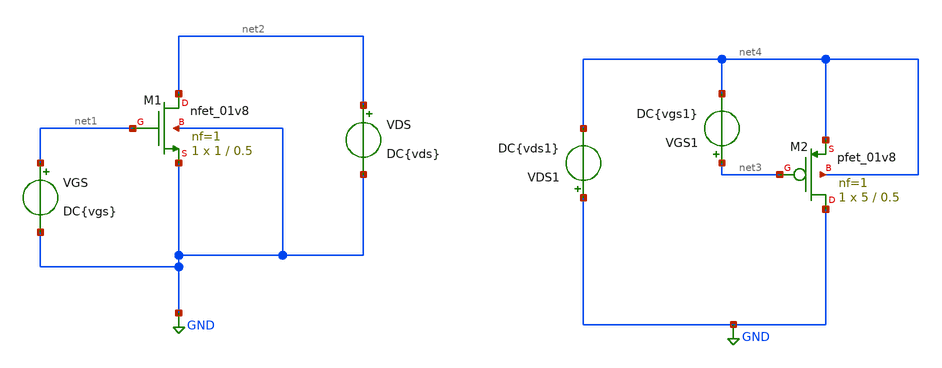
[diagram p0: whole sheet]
** sch_path: analog/mixer/nmos_vs_pmos.sch
**.subckt nmos_vs_pmos
VGS net1 GND DC{vgs}
VDS net2 GND DC{vds}
XM1 net2 net1 GND GND sky130_fd_pr__nfet_01v8 L=0.5 W=1 nf=1 ad='int((1 + 1)/2) * 1 / 1 * 0.29' as='int((1 + 2)/2) * 1 / 1 * 0.29'
+ pd='2*int((1 + 1)/2) * (1 / 1 + 0.29)' ps='2*int((1 + 2)/2) * (1 / 1 + 0.29)' nrd='0.29 / 1 ' nrs='0.29 / 1 '
+ sa=0 sb=0 sd=0 mult=1 m=1
XM2 GND net3 net4 net4 sky130_fd_pr__pfet_01v8 L=0.5 W=5 nf=1 ad='int((1 + 1)/2) * 5 / 1 * 0.29' as='int((1 + 2)/2) * 5 / 1 * 0.29'
+ pd='2*int((1 + 1)/2) * (5 / 1 + 0.29)' ps='2*int((1 + 2)/2) * (5 / 1 + 0.29)' nrd='0.29 / 5 ' nrs='0.29 / 5 '
+ sa=0 sb=0 sd=0 mult=1 m=1
VGS1 net3 net4 DC{vgs1}
VDS1 GND net4 DC{vds1}
**** begin user architecture code



* Parameters
.param vds = 1.8
.param vgs = 0.9
.param vds1 = -1.8
.param vgs1 = -0.9
.options TEMPS = 27.0

* Models
.lib /usr/local/share/pdk/sky130A/libs.tech/ngspice/sky130.lib.spice tt

* Data to save
.save all  @M.XM1.msky130_fd_pr__nfet_01v8[id]  @M.XM1.msky130_fd_pr__nfet_01v8[gm]  @M.XM1.msky130_fd_pr__nfet_01v8[vth]  @M.XM1.msky130_fd_pr__nfet_01v8[vds]  @M.XM1.msky130_fd_pr__nfet_01v8[vdsat]  @M.XM1.msky130_fd_pr__nfet_01v8[vgs]  @M.XM1.msky130_fd_pr__nfet_01v8[cgg]
  @M.XM2.msky130_fd_pr__pfet_01v8[id]  @M.XM2.msky130_fd_pr__pfet_01v8[gm]
+  @M.XM2.msky130_fd_pr__pfet_01v8[vth]  @M.XM2.msky130_fd_pr__pfet_01v8[vds]  @M.XM2.msky130_fd_pr__pfet_01v8[vdsat]
+  @M.XM2.msky130_fd_pr__pfet_01v8[vgs]  @M.XM2.msky130_fd_pr__pfet_01v8[cgg]



* Simulation
.control
  * Simulación para el NMOS (XM1)
  dc VDS 0 1.8 0.01 VGS 0 1.8 0.3
  plot @M.XM1.msky130_fd_pr__nfet_01v8[id] ylabel 'Id' xlabel 'Vds' title 'NMOS: L=0.5um W=1um'

  * Simulación para el PMOS (XM2)
  * Nota: Barremos de 0 a -1.8 para el PMOS
  dc VDS1 0 -1.8 -0.01 VGS1 0 -1.8 -0.3

  plot @M.XM2.msky130_fd_pr__pfet_01v8[id] ylabel 'Id' xlabel 'Vds' title 'PMOS: L=0.5um W=5um'

.endc
.end


**** end user architecture code
**.ends
.GLOBAL GND
.end
